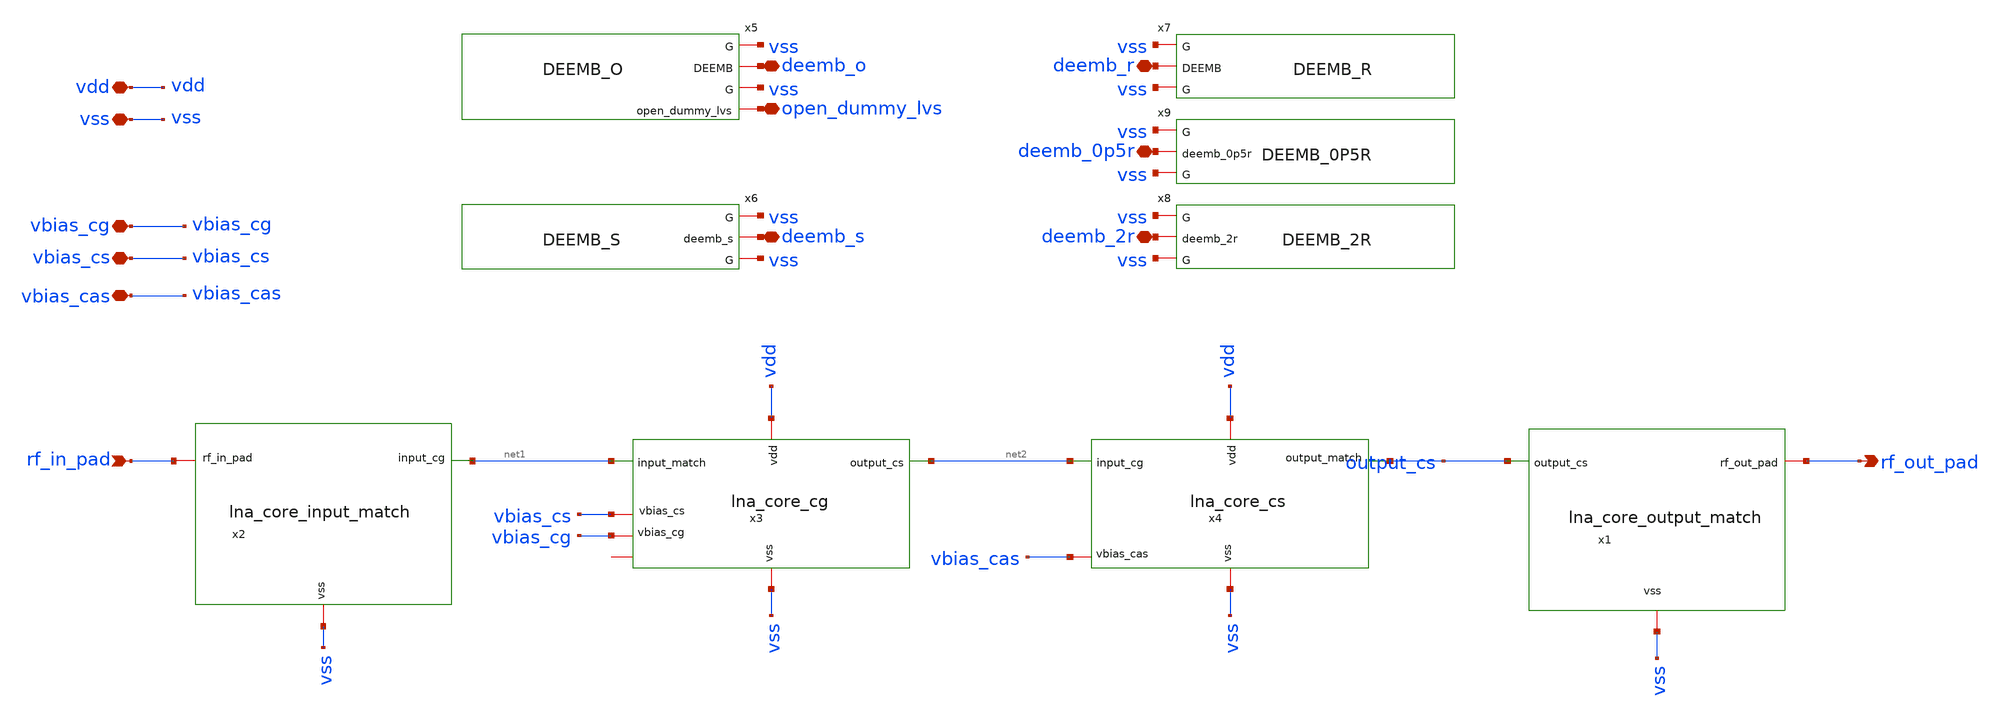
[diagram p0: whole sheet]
** sch_path: xschem/lna_core_parts.sch
**.subckt lna_core_parts rf_in_pad vbias_cg vbias_cs rf_out_pad vdd vss vbias_cas deemb_o deemb_s
*+ deemb_2r deemb_0p5r deemb_r open_dummy_lvs
*.ipin rf_in_pad
*.iopin vbias_cg
*.iopin vbias_cs
*.opin rf_out_pad
*.iopin vdd
*.iopin vss
*.iopin vbias_cas
*.iopin deemb_o
*.iopin deemb_s
*.iopin deemb_2r
*.iopin deemb_0p5r
*.iopin deemb_r
*.iopin open_dummy_lvs
x1 output_cs rf_out_pad vss lna_core_output_match
x2 vss net1 rf_in_pad lna_core_input_match
x3 vbias_cs vdd vss vbias_cg net2 net1 lna_core_cg
x4 output_cs vbias_cas net2 vdd vss lna_core_cs
x5 vss deemb_o open_dummy_lvs DEEMB_O
x6 vss deemb_s DEEMB_S
x7 vss deemb_r DEEMB_R
x8 vss deemb_2r DEEMB_2R
x9 vss deemb_0p5r DEEMB_0P5R
**** begin user architecture code

* LVS-only: every coil in this hierarchy is flattened directly into its own
* metal-resistor stand-in at the point of use (see lna_core_cg.sch,
* lna_core_cs.sch, lna_core_input_match.sch, lna_core_output_match.sch) --
* no subcircuit boundary, tied straight to the real nets, so the official
* gf180mcu.lvs engine has something comparable to match against the
* layout's resistor-marker geometry (see xschem/*_model.lib for the other
* ideal/rl/snp2le simulation variants, untouched by this selection).

**** end user architecture code
**.ends
.end
